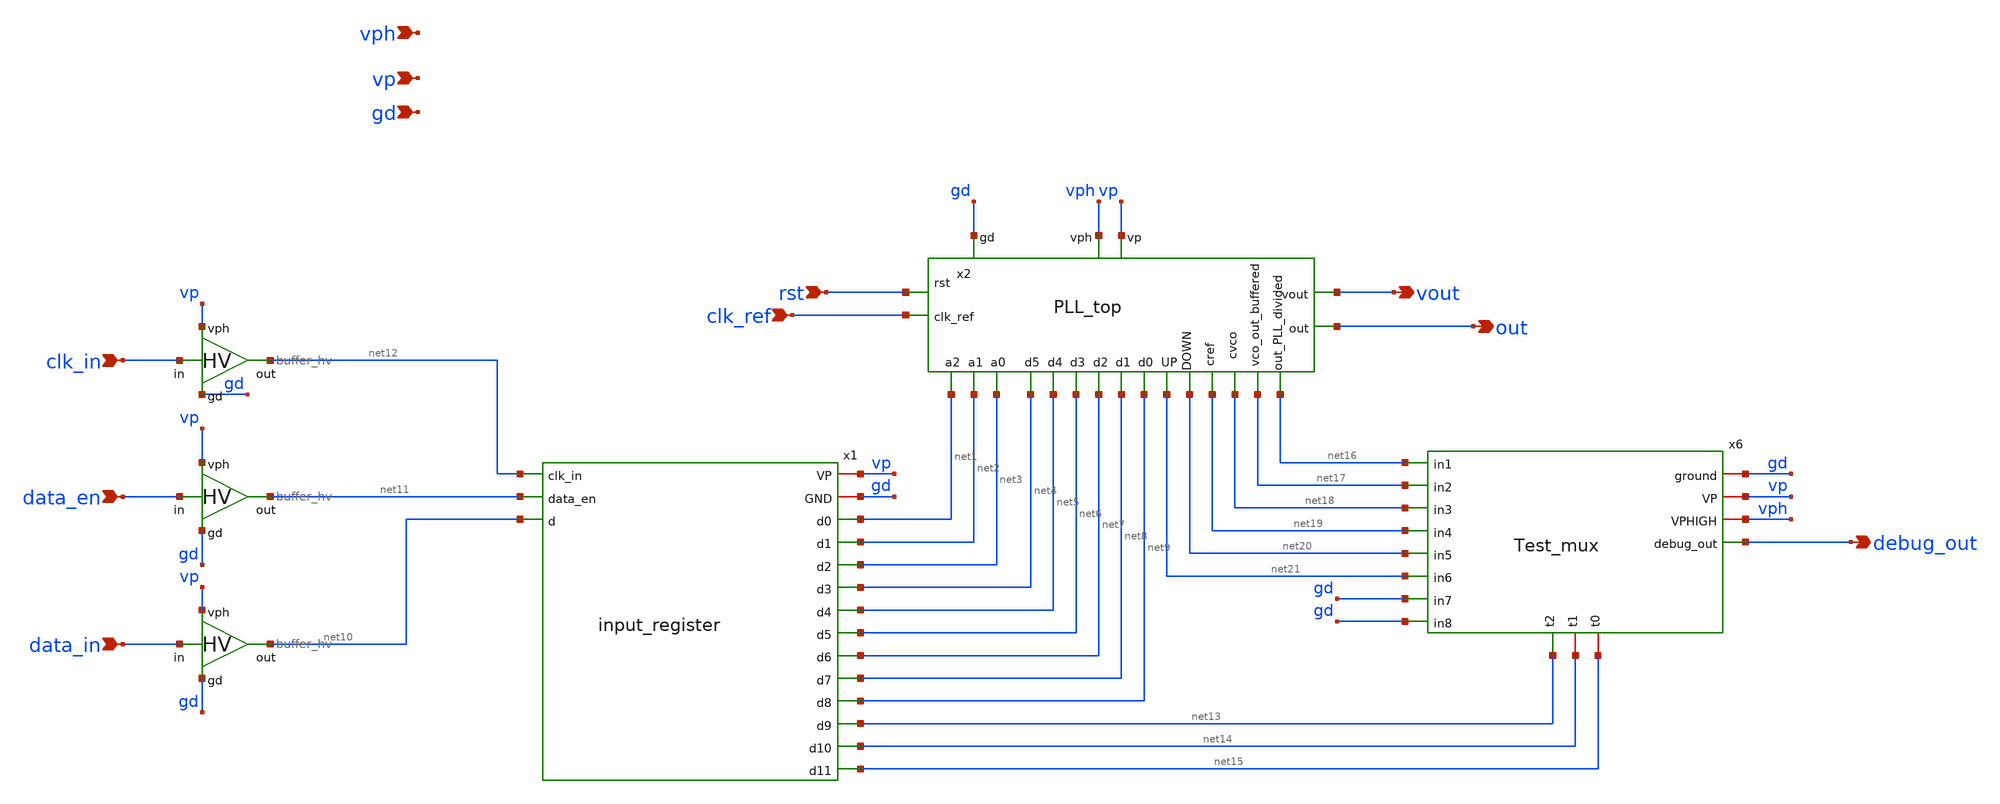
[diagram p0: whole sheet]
** sch_path: PLL0663-main/schematic/xschem/top/chip_top.sch
**.subckt chip_top vp gd clk_in data_en data_in clk_ref rst out vout vph debug_out
*.ipin vp
*.ipin gd
*.ipin clk_in
*.ipin data_en
*.ipin data_in
*.ipin clk_ref
*.ipin rst
*.opin out
*.opin vout
*.ipin vph
*.opin debug_out
x2 vp vph gd clk_ref out net4 net6 net2 net7 net8 net9 net5 net1 net3 rst vout net19 net21 net20
+ net18 net17 net16 PLL_top
x1 vp gd net12 net11 net10 net1 net2 net3 net4 net5 net6 net7 net8 net9 net13 net14 net15
+ input_register
x3 vp data_in net10 gd buffer_hv
x4 vp data_en net11 gd buffer_hv
x5 vp clk_in net12 gd buffer_hv
x6 net15 net14 net13 gd vp debug_out net16 net17 net18 net19 net20 net21 gd gd vph Test_mux
**.ends
.end
